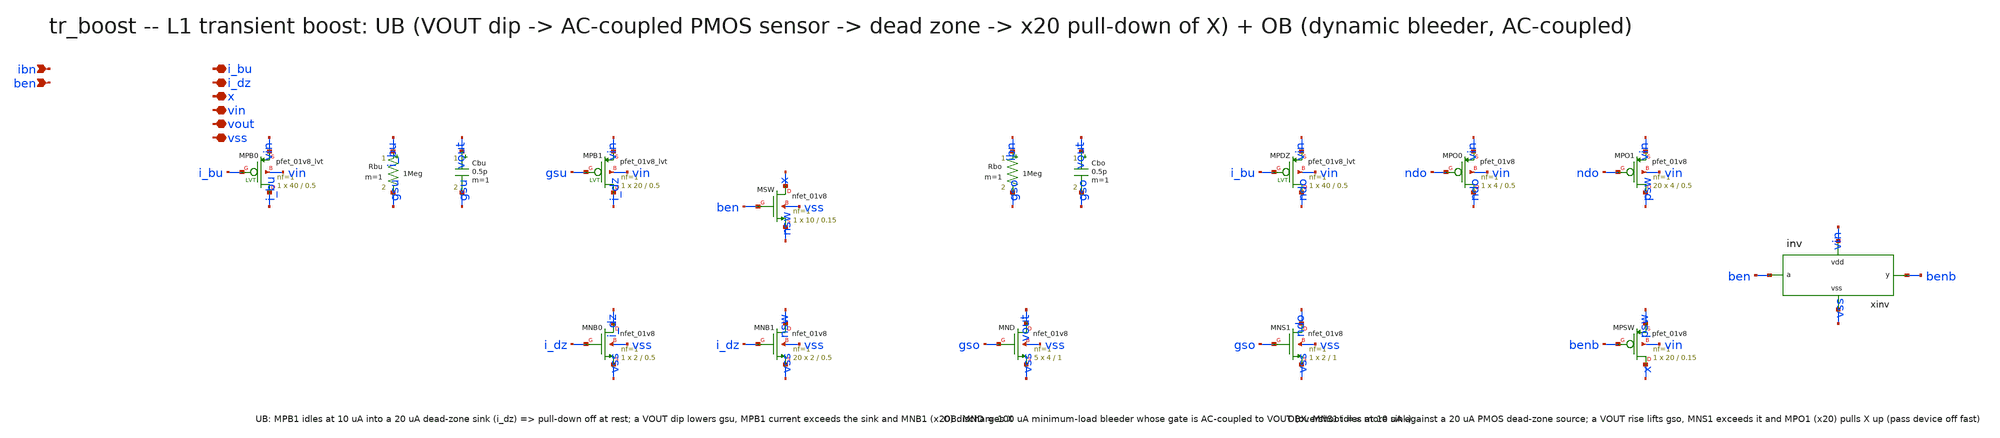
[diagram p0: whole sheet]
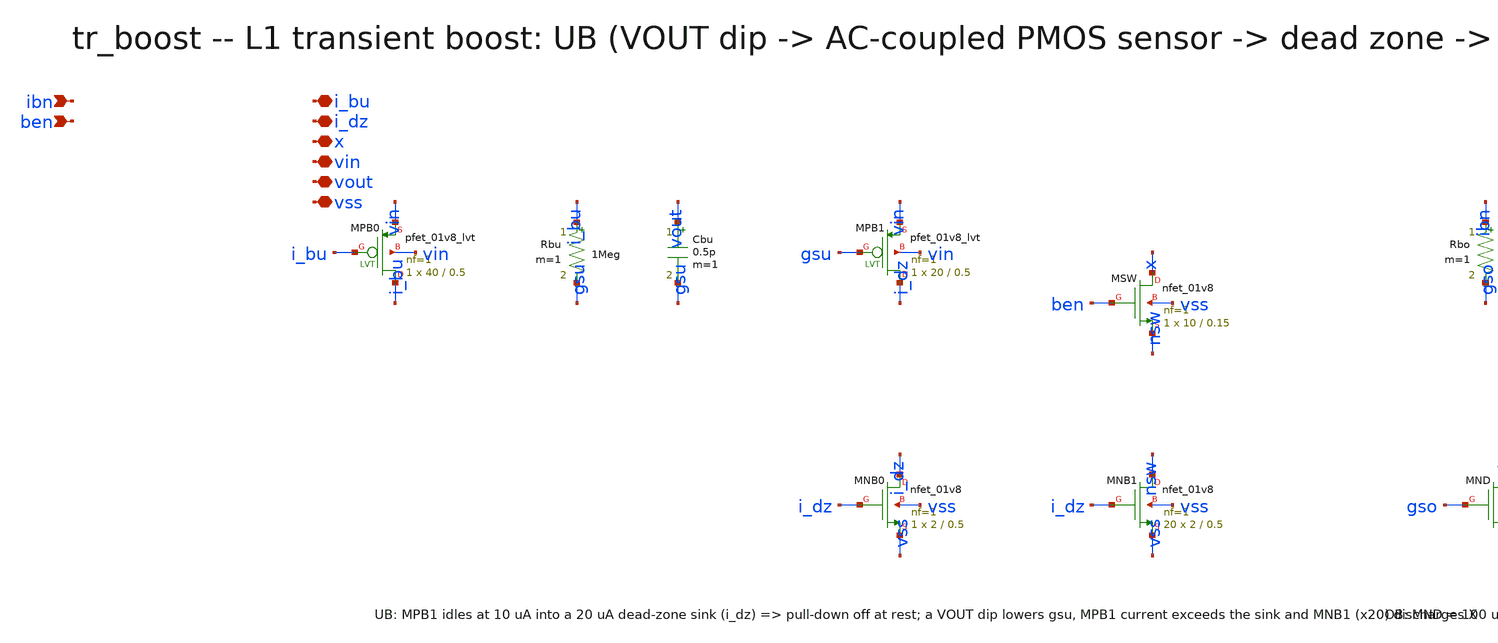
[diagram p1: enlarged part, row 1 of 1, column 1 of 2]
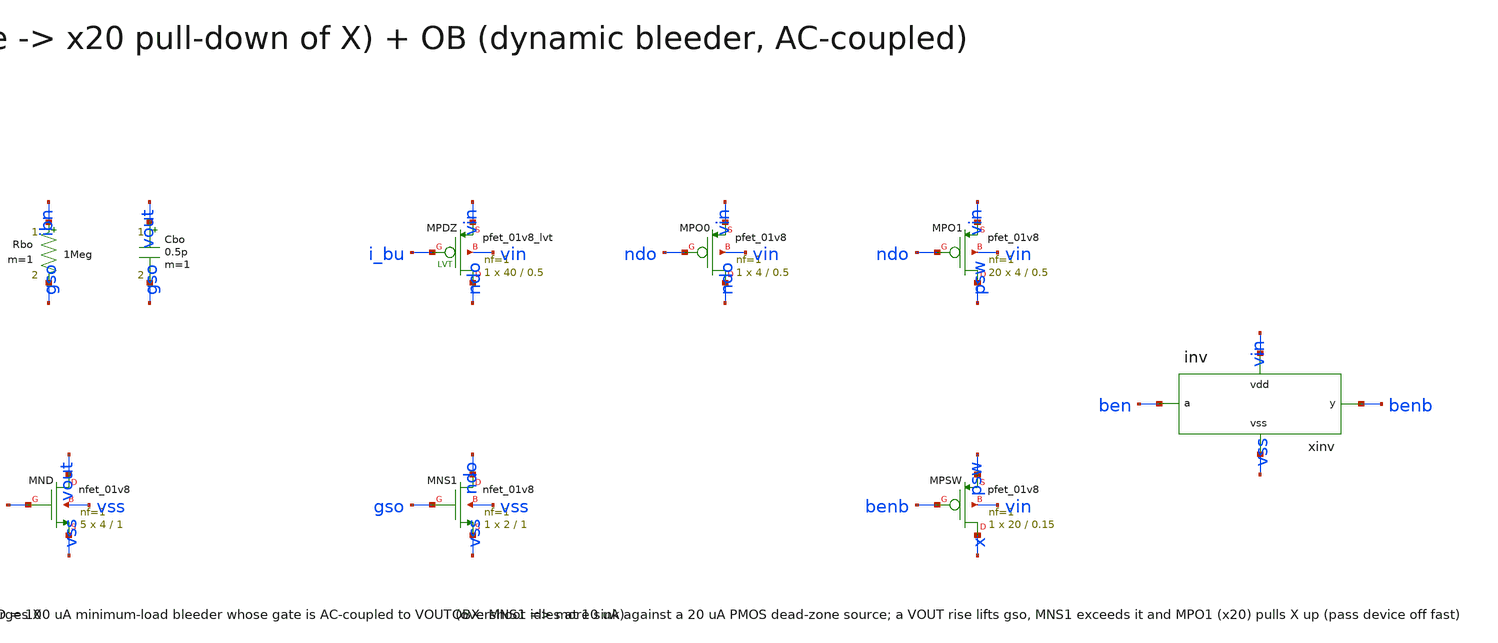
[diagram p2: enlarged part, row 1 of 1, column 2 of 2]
** sch_path: xschem/onetops/tr_boost.sch
**.subckt tr_boost ibn ben i_bu i_dz x vin vout vss
*.ipin ibn
*.ipin ben
*.iopin i_bu
*.iopin i_dz
*.iopin x
*.iopin vin
*.iopin vout
*.iopin vss
XMPB0 i_bu i_bu vin vin sky130_fd_pr__pfet_01v8_lvt L=0.5 W=40 nf=1 ad='int((1 + 1)/2) * 40 / 1 * 0.29'
+ as='int((1 + 2)/2) * 40 / 1 * 0.29' pd='2*int((1 + 1)/2) * (40 / 1 + 0.29)' ps='2*int((1 + 2)/2) * (40 / 1 + 0.29)'
+ nrd='0.29 / 40 ' nrs='0.29 / 40 ' sa=0 sb=0 sd=0 mult=1 m=1
Rbu i_bu gsu 1Meg m=1
Cbu vout gsu 0.5p m=1
XMPB1 i_dz gsu vin vin sky130_fd_pr__pfet_01v8_lvt L=0.5 W=20 nf=1 ad='int((1 + 1)/2) * 20 / 1 * 0.29'
+ as='int((1 + 2)/2) * 20 / 1 * 0.29' pd='2*int((1 + 1)/2) * (20 / 1 + 0.29)' ps='2*int((1 + 2)/2) * (20 / 1 + 0.29)'
+ nrd='0.29 / 20 ' nrs='0.29 / 20 ' sa=0 sb=0 sd=0 mult=1 m=1
XMNB0 i_dz i_dz vss vss sky130_fd_pr__nfet_01v8 L=0.5 W=2 nf=1 ad='int((1 + 1)/2) * 2 / 1 * 0.29' as='int((1 + 2)/2) * 2 / 1 * 0.29'
+ pd='2*int((1 + 1)/2) * (2 / 1 + 0.29)' ps='2*int((1 + 2)/2) * (2 / 1 + 0.29)' nrd='0.29 / 2 ' nrs='0.29 / 2 '
+ sa=0 sb=0 sd=0 mult=1 m=1
XMNB1 nsw i_dz vss vss sky130_fd_pr__nfet_01v8 L=0.5 W=2 nf=1 ad='int((1 + 1)/2) * 2 / 1 * 0.29' as='int((1 + 2)/2) * 2 / 1 * 0.29'
+ pd='2*int((1 + 1)/2) * (2 / 1 + 0.29)' ps='2*int((1 + 2)/2) * (2 / 1 + 0.29)' nrd='0.29 / 2 ' nrs='0.29 / 2 '
+ sa=0 sb=0 sd=0 mult=20 m=20
XMSW x ben nsw vss sky130_fd_pr__nfet_01v8 L=0.15 W=10 nf=1 ad='int((1 + 1)/2) * 10 / 1 * 0.29' as='int((1 + 2)/2) * 10 / 1 * 0.29'
+ pd='2*int((1 + 1)/2) * (10 / 1 + 0.29)' ps='2*int((1 + 2)/2) * (10 / 1 + 0.29)' nrd='0.29 / 10 ' nrs='0.29 / 10 '
+ sa=0 sb=0 sd=0 mult=1 m=1
Rbo ibn gso 1Meg m=1
Cbo vout gso 0.5p m=1
XMND vout gso vss vss sky130_fd_pr__nfet_01v8 L=1 W=4 nf=1 ad='int((1 + 1)/2) * 4 / 1 * 0.29' as='int((1 + 2)/2) * 4 / 1 * 0.29'
+ pd='2*int((1 + 1)/2) * (4 / 1 + 0.29)' ps='2*int((1 + 2)/2) * (4 / 1 + 0.29)' nrd='0.29 / 4 ' nrs='0.29 / 4 '
+ sa=0 sb=0 sd=0 mult=5 m=5
XMPDZ ndo i_bu vin vin sky130_fd_pr__pfet_01v8_lvt L=0.5 W=40 nf=1 ad='int((1 + 1)/2) * 40 / 1 * 0.29'
+ as='int((1 + 2)/2) * 40 / 1 * 0.29' pd='2*int((1 + 1)/2) * (40 / 1 + 0.29)' ps='2*int((1 + 2)/2) * (40 / 1 + 0.29)'
+ nrd='0.29 / 40 ' nrs='0.29 / 40 ' sa=0 sb=0 sd=0 mult=1 m=1
XMNS1 ndo gso vss vss sky130_fd_pr__nfet_01v8 L=1 W=2 nf=1 ad='int((1 + 1)/2) * 2 / 1 * 0.29' as='int((1 + 2)/2) * 2 / 1 * 0.29'
+ pd='2*int((1 + 1)/2) * (2 / 1 + 0.29)' ps='2*int((1 + 2)/2) * (2 / 1 + 0.29)' nrd='0.29 / 2 ' nrs='0.29 / 2 '
+ sa=0 sb=0 sd=0 mult=1 m=1
XMPO0 ndo ndo vin vin sky130_fd_pr__pfet_01v8 L=0.5 W=4 nf=1 ad='int((1 + 1)/2) * 4 / 1 * 0.29' as='int((1 + 2)/2) * 4 / 1 * 0.29'
+ pd='2*int((1 + 1)/2) * (4 / 1 + 0.29)' ps='2*int((1 + 2)/2) * (4 / 1 + 0.29)' nrd='0.29 / 4 ' nrs='0.29 / 4 '
+ sa=0 sb=0 sd=0 mult=1 m=1
XMPO1 psw ndo vin vin sky130_fd_pr__pfet_01v8 L=0.5 W=4 nf=1 ad='int((1 + 1)/2) * 4 / 1 * 0.29' as='int((1 + 2)/2) * 4 / 1 * 0.29'
+ pd='2*int((1 + 1)/2) * (4 / 1 + 0.29)' ps='2*int((1 + 2)/2) * (4 / 1 + 0.29)' nrd='0.29 / 4 ' nrs='0.29 / 4 '
+ sa=0 sb=0 sd=0 mult=20 m=20
XMPSW x benb psw vin sky130_fd_pr__pfet_01v8 L=0.15 W=20 nf=1 ad='int((1 + 1)/2) * 20 / 1 * 0.29' as='int((1 + 2)/2) * 20 / 1 * 0.29'
+ pd='2*int((1 + 1)/2) * (20 / 1 + 0.29)' ps='2*int((1 + 2)/2) * (20 / 1 + 0.29)' nrd='0.29 / 20 ' nrs='0.29 / 20 '
+ sa=0 sb=0 sd=0 mult=1 m=1
xinv ben benb vin vss inv
**.ends

* expanding   symbol:  onetops/inv.sym # of pins=4
** sym_path: xschem/onetops/inv.sym
** sch_path: xschem/onetops/inv.sch
.subckt inv a y vdd vss
*.ipin a
*.opin y
*.iopin vdd
*.iopin vss
XMP1 y a vdd vdd sky130_fd_pr__pfet_01v8 L=0.15 W=2 nf=1 ad='int((1 + 1)/2) * 2 / 1 * 0.29' as='int((1 + 2)/2) * 2 / 1 * 0.29'
+ pd='2*int((1 + 1)/2) * (2 / 1 + 0.29)' ps='2*int((1 + 2)/2) * (2 / 1 + 0.29)' nrd='0.29 / 2 ' nrs='0.29 / 2 '
+ sa=0 sb=0 sd=0 mult=1 m=1
XMN1 y a vss vss sky130_fd_pr__nfet_01v8 L=0.15 W=1 nf=1 ad='int((1 + 1)/2) * 1 / 1 * 0.29' as='int((1 + 2)/2) * 1 / 1 * 0.29'
+ pd='2*int((1 + 1)/2) * (1 / 1 + 0.29)' ps='2*int((1 + 2)/2) * (1 / 1 + 0.29)' nrd='0.29 / 1 ' nrs='0.29 / 1 '
+ sa=0 sb=0 sd=0 mult=1 m=1
.ends

.end
